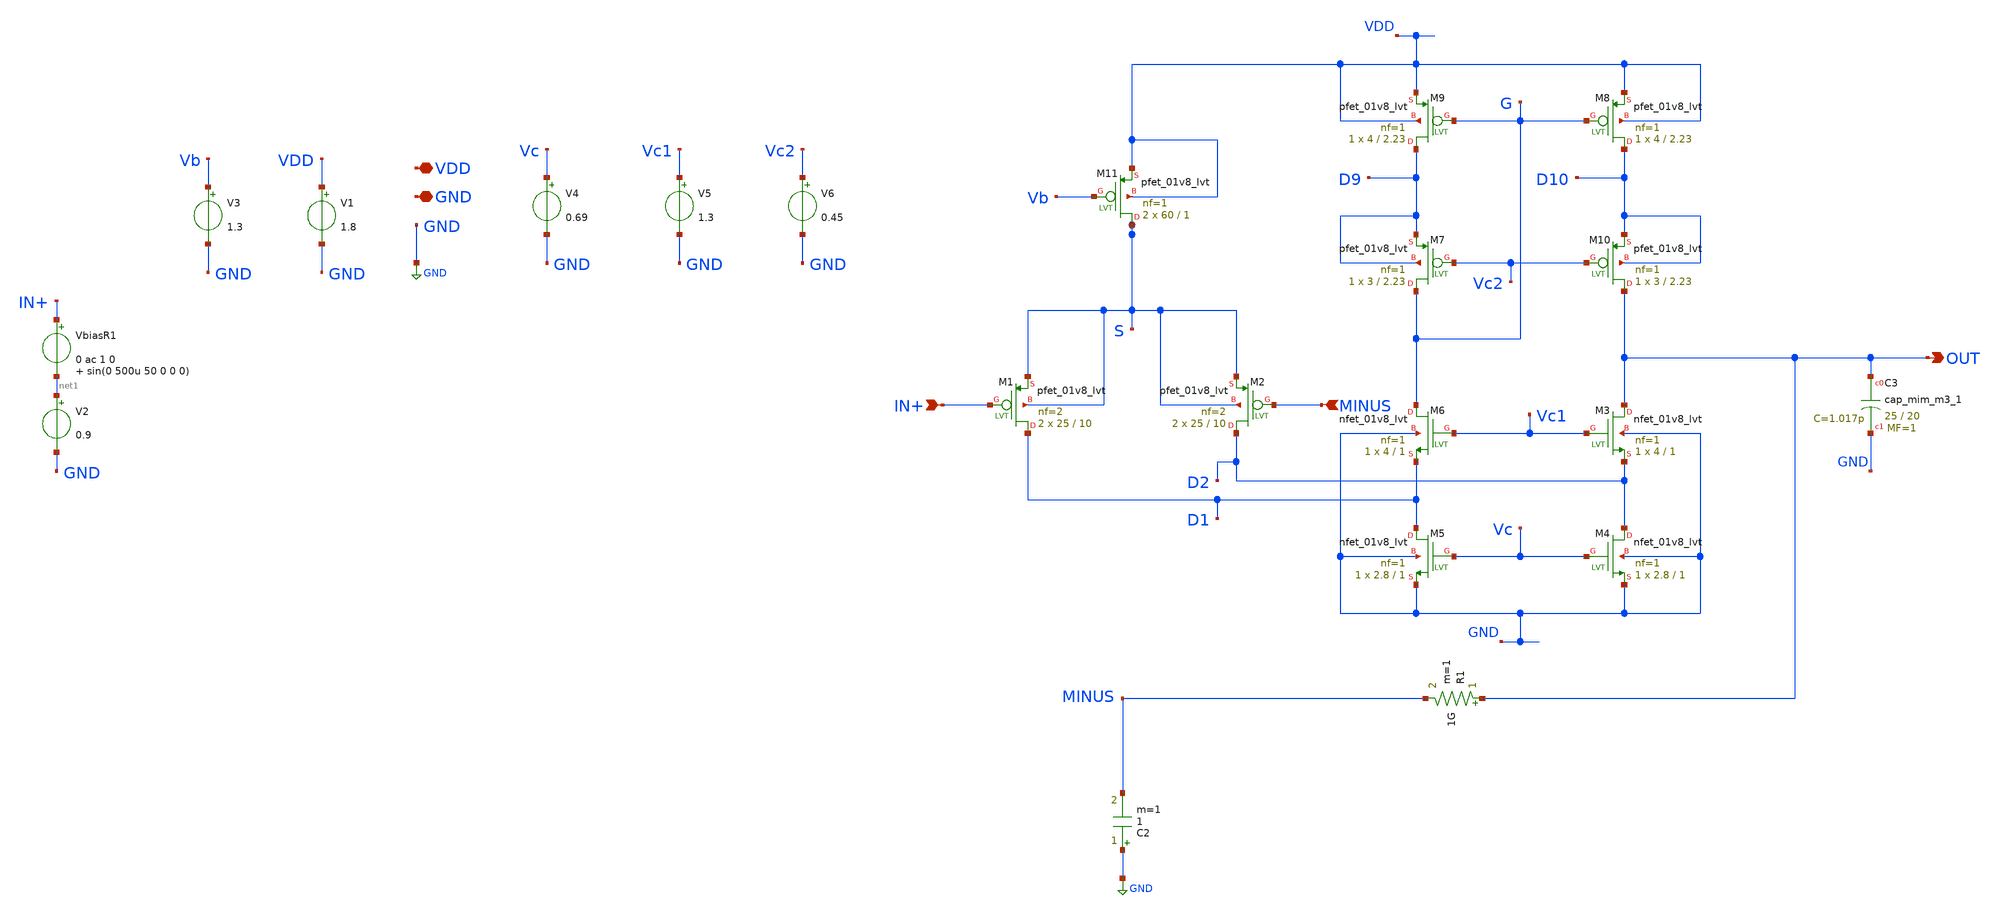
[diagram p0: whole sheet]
** sch_path: xschem/OTA_FoldedCascode_Noise1.sch
**.subckt OTA_FoldedCascode_Noise1 OUT VDD GND IN+ MINUS
*.opin OUT
*.iopin VDD
*.iopin GND
*.ipin IN+
*.ipin MINUS
VbiasR1 IN+ net1 0 ac 1 0 sin(0 500u 50 0 0 0)
V2 net1 GND 0.9
XC3 OUT GND sky130_fd_pr__cap_mim_m3_1 W=25 L=20 MF=1 m=1
C2 GND MINUS 1 m=1
R1 OUT MINUS 1G m=1
V1 VDD GND 1.8
XM11 S Vb VDD VDD sky130_fd_pr__pfet_01v8_lvt L=1 W=60 nf=1 ad='int((nf+1)/2) * W/nf * 0.29' as='int((nf+2)/2) * W/nf * 0.29'
+ pd='2*int((nf+1)/2) * (W/nf + 0.29)' ps='2*int((nf+2)/2) * (W/nf + 0.29)' nrd='0.29 / W' nrs='0.29 / W'
+ sa=0 sb=0 sd=0 mult=2 m=2
V3 Vb GND 1.3
XM1 D1 IN+ S S sky130_fd_pr__pfet_01v8_lvt L=10 W=25 nf=2 ad='int((nf+1)/2) * W/nf * 0.29' as='int((nf+2)/2) * W/nf * 0.29'
+ pd='2*int((nf+1)/2) * (W/nf + 0.29)' ps='2*int((nf+2)/2) * (W/nf + 0.29)' nrd='0.29 / W' nrs='0.29 / W'
+ sa=0 sb=0 sd=0 mult=2 m=2
XM2 D2 MINUS S S sky130_fd_pr__pfet_01v8_lvt L=10 W=25 nf=2 ad='int((nf+1)/2) * W/nf * 0.29' as='int((nf+2)/2) * W/nf * 0.29'
+ pd='2*int((nf+1)/2) * (W/nf + 0.29)' ps='2*int((nf+2)/2) * (W/nf + 0.29)' nrd='0.29 / W' nrs='0.29 / W'
+ sa=0 sb=0 sd=0 mult=2 m=2
XM3 OUT Vc1 D2 GND sky130_fd_pr__nfet_01v8_lvt L=1 W=4 nf=1 ad='int((nf+1)/2) * W/nf * 0.29' as='int((nf+2)/2) * W/nf * 0.29'
+ pd='2*int((nf+1)/2) * (W/nf + 0.29)' ps='2*int((nf+2)/2) * (W/nf + 0.29)' nrd='0.29 / W' nrs='0.29 / W'
+ sa=0 sb=0 sd=0 mult=1 m=1
XM4 D2 Vc GND GND sky130_fd_pr__nfet_01v8_lvt L=1 W=2.8 nf=1 ad='int((nf+1)/2) * W/nf * 0.29' as='int((nf+2)/2) * W/nf * 0.29'
+ pd='2*int((nf+1)/2) * (W/nf + 0.29)' ps='2*int((nf+2)/2) * (W/nf + 0.29)' nrd='0.29 / W' nrs='0.29 / W'
+ sa=0 sb=0 sd=0 mult=1 m=1
XM5 D1 Vc GND GND sky130_fd_pr__nfet_01v8_lvt L=1 W=2.8 nf=1 ad='int((nf+1)/2) * W/nf * 0.29' as='int((nf+2)/2) * W/nf * 0.29'
+ pd='2*int((nf+1)/2) * (W/nf + 0.29)' ps='2*int((nf+2)/2) * (W/nf + 0.29)' nrd='0.29 / W' nrs='0.29 / W'
+ sa=0 sb=0 sd=0 mult=1 m=1
XM6 G Vc1 D1 GND sky130_fd_pr__nfet_01v8_lvt L=1 W=4 nf=1 ad='int((nf+1)/2) * W/nf * 0.29' as='int((nf+2)/2) * W/nf * 0.29'
+ pd='2*int((nf+1)/2) * (W/nf + 0.29)' ps='2*int((nf+2)/2) * (W/nf + 0.29)' nrd='0.29 / W' nrs='0.29 / W'
+ sa=0 sb=0 sd=0 mult=1 m=1
V4 Vc GND 0.69
V5 Vc1 GND 1.3
XM7 G Vc2 D9 D9 sky130_fd_pr__pfet_01v8_lvt L=2.23 W=3 nf=1 ad='int((nf+1)/2) * W/nf * 0.29' as='int((nf+2)/2) * W/nf * 0.29'
+ pd='2*int((nf+1)/2) * (W/nf + 0.29)' ps='2*int((nf+2)/2) * (W/nf + 0.29)' nrd='0.29 / W' nrs='0.29 / W'
+ sa=0 sb=0 sd=0 mult=1 m=1
XM9 D9 G VDD VDD sky130_fd_pr__pfet_01v8_lvt L=2.23 W=4 nf=1 ad='int((nf+1)/2) * W/nf * 0.29' as='int((nf+2)/2) * W/nf * 0.29'
+ pd='2*int((nf+1)/2) * (W/nf + 0.29)' ps='2*int((nf+2)/2) * (W/nf + 0.29)' nrd='0.29 / W' nrs='0.29 / W'
+ sa=0 sb=0 sd=0 mult=1 m=1
XM8 D10 G VDD VDD sky130_fd_pr__pfet_01v8_lvt L=2.23 W=4 nf=1 ad='int((nf+1)/2) * W/nf * 0.29' as='int((nf+2)/2) * W/nf * 0.29'
+ pd='2*int((nf+1)/2) * (W/nf + 0.29)' ps='2*int((nf+2)/2) * (W/nf + 0.29)' nrd='0.29 / W' nrs='0.29 / W'
+ sa=0 sb=0 sd=0 mult=1 m=1
XM10 OUT Vc2 D10 D10 sky130_fd_pr__pfet_01v8_lvt L=2.23 W=3 nf=1 ad='int((nf+1)/2) * W/nf * 0.29' as='int((nf+2)/2) * W/nf * 0.29'
+ pd='2*int((nf+1)/2) * (W/nf + 0.29)' ps='2*int((nf+2)/2) * (W/nf + 0.29)' nrd='0.29 / W' nrs='0.29 / W'
+ sa=0 sb=0 sd=0 mult=1 m=1
V6 Vc2 GND 0.45
**** begin user architecture code



.option reltol=1e-5   abstol=1e-14 savecurrents
.control
  save all
  op
  remzerovec
  write OTA_FoldedCascode_Noise1.raw

  set appendwrite
  noise v(out) VbiasR1 dec 10 0.5 1e3
  remzerovec
  write OTA_FoldedCascode_Noise1.raw
  setplot noise1
  plot inoise_spectrum

.endc



.lib $::SKYWATER_MODELS/sky130.lib.spice tt
**** end user architecture code
**.ends
.GLOBAL GND
.end
